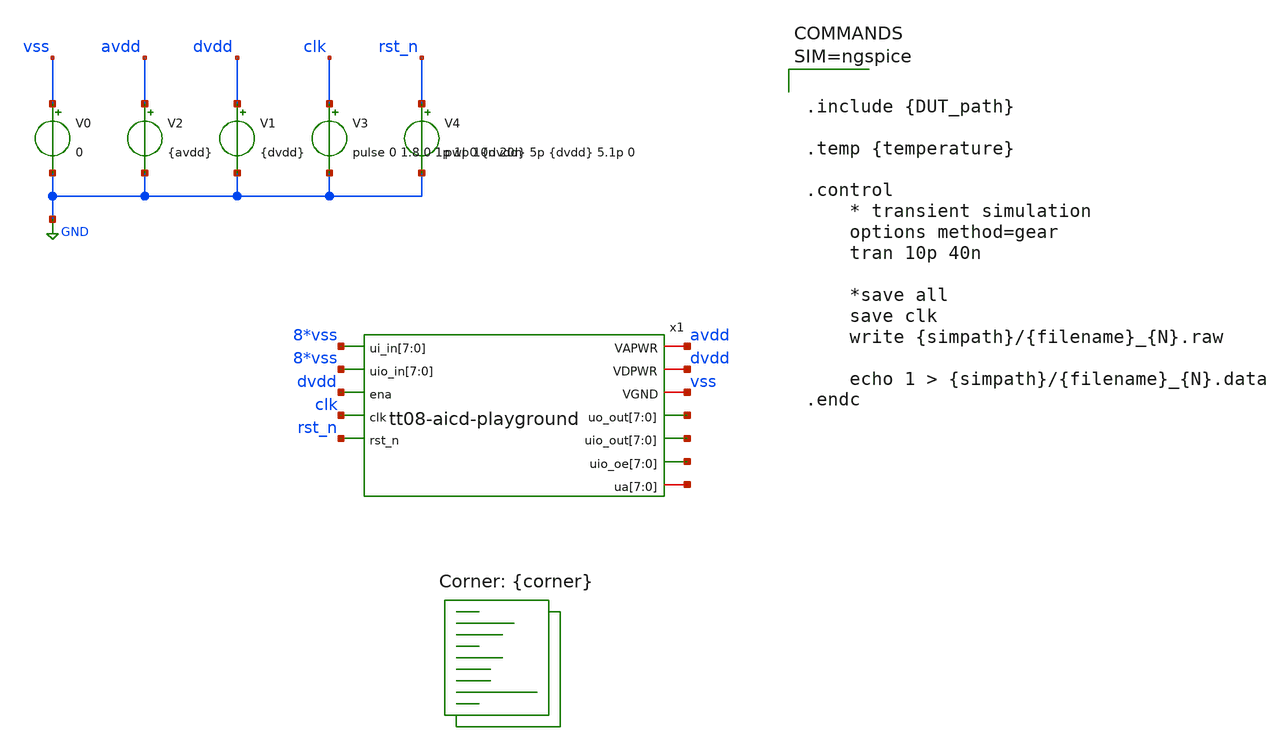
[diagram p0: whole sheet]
** sch_path: cace/templates/transient_tb.sch
**.subckt transient_tb
x1 avdd vss vss vss vss vss vss vss vss dvdd vss vss vss vss vss vss vss vss vss dvdd net1[7]
+ net1[6] net1[5] net1[4] net1[3] net1[2] net1[1] net1[0] clk rst_n net2[7] net2[6] net2[5] net2[4] net2[3]
+ net2[2] net2[1] net2[0] net3[7] net3[6] net3[5] net3[4] net3[3] net3[2] net3[1] net3[0] net4[7] net4[6]
+ net4[5] net4[4] net4[3] net4[2] net4[1] net4[0] tt08-aicd-playground
V0 vss GND 0
V2 avdd GND {avdd}
V1 dvdd GND {dvdd}
V3 clk GND pulse 0 1.8 0 1p 1p 10n 20n
V4 rst_n GND pwl 0 {dvdd} 5p {dvdd} 5.1p 0
**** begin user architecture code
.lib $::SKYWATER_MODELS/sky130.lib.spice {corner}



.include {DUT_path}

.temp {temperature}

.control
    * transient simulation
    options method=gear
    tran 10p 40n

    *save all
    save clk
    write {simpath}/{filename}_{N}.raw

    echo 1 > {simpath}/{filename}_{N}.data
.endc



**** end user architecture code
**.ends
.GLOBAL GND
.end
